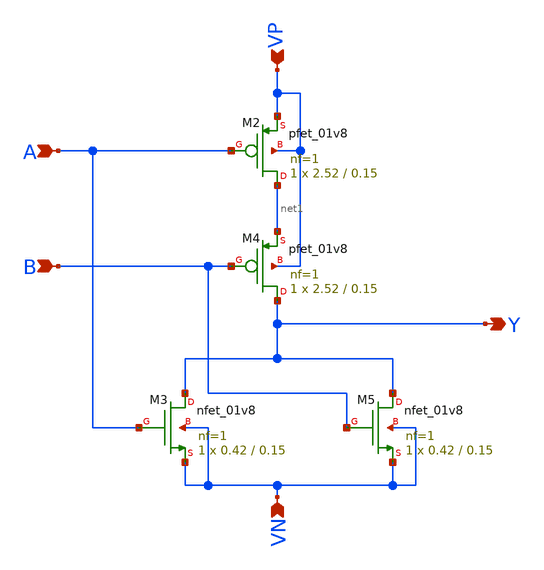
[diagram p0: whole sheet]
** sch_path: component/NOR2/NOR2.sch
**.subckt NOR2 Y A B VP VN
*.opin Y
*.ipin A
*.ipin B
*.ipin VP
*.ipin VN
XM5 Y B VN VN sky130_fd_pr__nfet_01v8 L=0.15 W=0.42 nf=1 ad='int((nf+1)/2) * W/nf * 0.29' as='int((nf+2)/2) * W/nf * 0.29'
+ pd='2*int((nf+1)/2) * (W/nf + 0.29)' ps='2*int((nf+2)/2) * (W/nf + 0.29)' nrd='0.29 / W' nrs='0.29 / W'
+ sa=0 sb=0 sd=0 mult=1 m=1
XM3 Y A VN VN sky130_fd_pr__nfet_01v8 L=0.15 W=0.42 nf=1 ad='int((nf+1)/2) * W/nf * 0.29' as='int((nf+2)/2) * W/nf * 0.29'
+ pd='2*int((nf+1)/2) * (W/nf + 0.29)' ps='2*int((nf+2)/2) * (W/nf + 0.29)' nrd='0.29 / W' nrs='0.29 / W'
+ sa=0 sb=0 sd=0 mult=1 m=1
XM2 net1 A VP VP sky130_fd_pr__pfet_01v8 L=0.15 W=2.52 nf=1 ad='int((nf+1)/2) * W/nf * 0.29' as='int((nf+2)/2) * W/nf * 0.29'
+ pd='2*int((nf+1)/2) * (W/nf + 0.29)' ps='2*int((nf+2)/2) * (W/nf + 0.29)' nrd='0.29 / W' nrs='0.29 / W'
+ sa=0 sb=0 sd=0 mult=1 m=1
XM4 Y B net1 VP sky130_fd_pr__pfet_01v8 L=0.15 W=2.52 nf=1 ad='int((nf+1)/2) * W/nf * 0.29' as='int((nf+2)/2) * W/nf * 0.29'
+ pd='2*int((nf+1)/2) * (W/nf + 0.29)' ps='2*int((nf+2)/2) * (W/nf + 0.29)' nrd='0.29 / W' nrs='0.29 / W'
+ sa=0 sb=0 sd=0 mult=1 m=1
**.ends
.end
